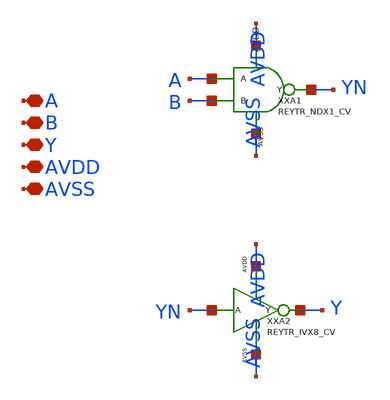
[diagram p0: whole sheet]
** sch_path: design/REY_TR_SKY130A/REYTR_ANX8_CV.sch
**.subckt REYTR_ANX8_CV A B Y AVDD AVSS
*.iopin A
*.iopin B
*.iopin Y
*.iopin AVDD
*.iopin AVSS
XXA1 A B YN AVDD AVSS REYTR_NDX1_CV
XXA2 AVSS AVDD YN Y REYTR_IVX8_CV
**.ends
.end
